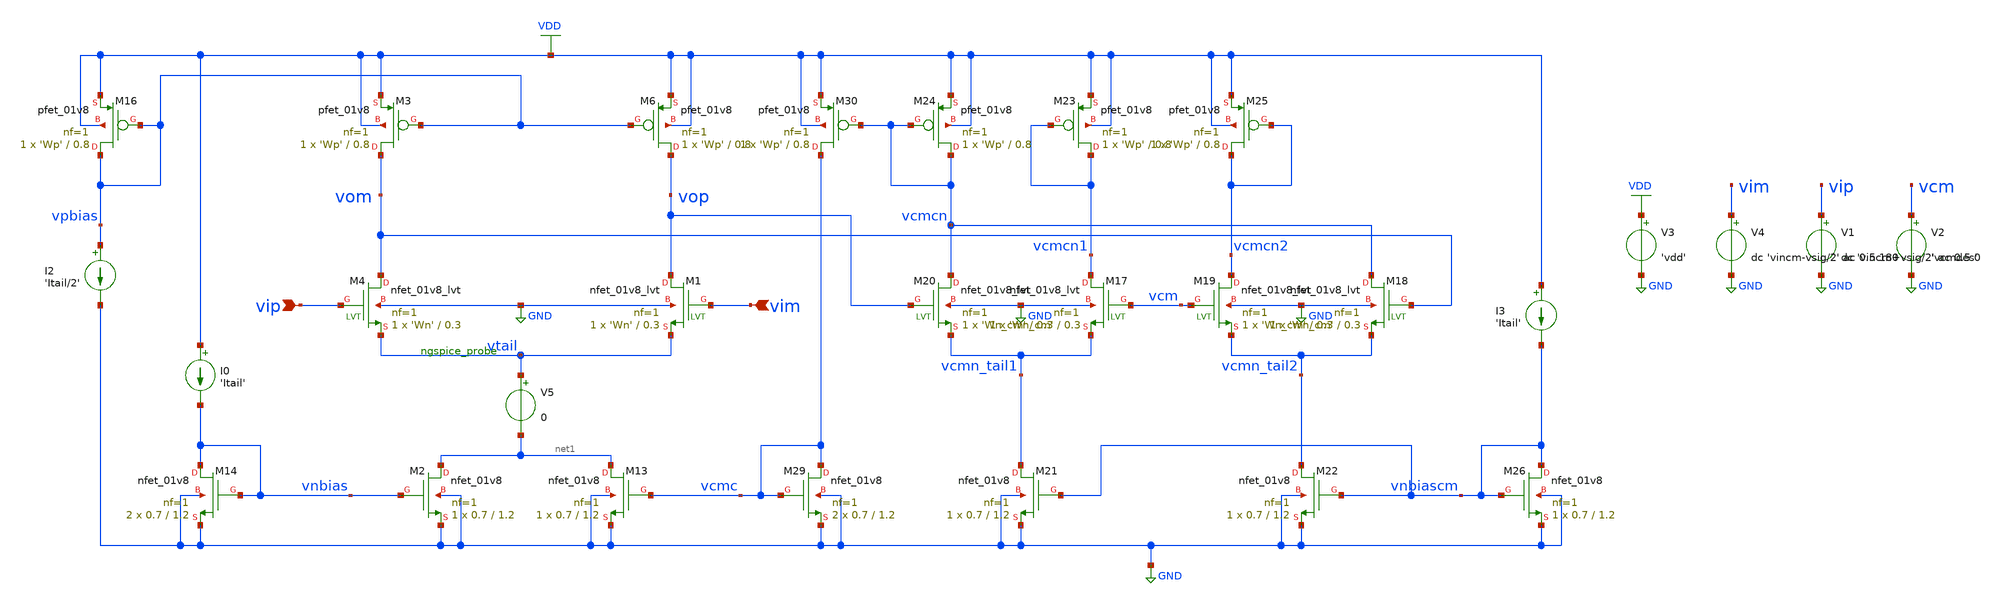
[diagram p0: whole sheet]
** sch_path: designs/diff_ota.sch
* Copyright 2020 Stefan Frederik Schippers
* Licensed under the Apache License, Version 2.0 (the "License");
* you may not use this file except in compliance with the License.
* You may obtain a copy of the License at
* https://www.apache.org/licenses/LICENSE-2.0
* Unless required by applicable law or agreed to in writing, software
* distributed under the License is distributed on an "AS IS" BASIS,
* WITHOUT WARRANTIES OR CONDITIONS OF ANY KIND, either express or implied.
* See the License for the specific language governing permissions and
* limitations under the License.
**.subckt diff_ota vip vim
*.ipin vip
*.ipin vim
V1 vip GND dc 'vincm+vsig/2' ac 0.5 0
V3 VDD GND 'vdd'
V4 vim GND dc 'vincm-vsig/2' ac 0.5 180
V5 vtail net1 0
XM6 vop vpbias VDD VDD sky130_fd_pr__pfet_01v8 L=0.8 W='Wp' nf=1 ad='int((nf+1)/2) * W/nf * 0.29' as='int((nf+2)/2) * W/nf * 0.29'
+ pd='2*int((nf+1)/2) * (W/nf + 0.29)' ps='2*int((nf+2)/2) * (W/nf + 0.29)' nrd='0.29 / W' nrs='0.29 / W'
+ sa=0 sb=0 sd=0 mult=1 m=1
XM3 vom vpbias VDD VDD sky130_fd_pr__pfet_01v8 L=0.8 W='Wp' nf=1 ad='int((nf+1)/2) * W/nf * 0.29' as='int((nf+2)/2) * W/nf * 0.29'
+ pd='2*int((nf+1)/2) * (W/nf + 0.29)' ps='2*int((nf+2)/2) * (W/nf + 0.29)' nrd='0.29 / W' nrs='0.29 / W'
+ sa=0 sb=0 sd=0 mult=1 m=1
XM2 net1 vnbias GND GND sky130_fd_pr__nfet_01v8 L=1.2 W=0.7 nf=1 ad='int((nf+1)/2) * W/nf * 0.29' as='int((nf+2)/2) * W/nf * 0.29'
+ pd='2*int((nf+1)/2) * (W/nf + 0.29)' ps='2*int((nf+2)/2) * (W/nf + 0.29)' nrd='0.29 / W' nrs='0.29 / W'
+ sa=0 sb=0 sd=0 mult=1 m=1
XM13 net1 vcmc GND GND sky130_fd_pr__nfet_01v8 L=1.2 W=0.7 nf=1 ad='int((nf+1)/2) * W/nf * 0.29' as='int((nf+2)/2) * W/nf * 0.29'
+ pd='2*int((nf+1)/2) * (W/nf + 0.29)' ps='2*int((nf+2)/2) * (W/nf + 0.29)' nrd='0.29 / W' nrs='0.29 / W'
+ sa=0 sb=0 sd=0 mult=1 m=1
I0 VDD vnbias 'Itail'
XM14 vnbias vnbias GND GND sky130_fd_pr__nfet_01v8 L=1.2 W=0.7 nf=1 ad='int((nf+1)/2) * W/nf * 0.29'
+ as='int((nf+2)/2) * W/nf * 0.29' pd='2*int((nf+1)/2) * (W/nf + 0.29)' ps='2*int((nf+2)/2) * (W/nf + 0.29)'
+ nrd='0.29 / W' nrs='0.29 / W' sa=0 sb=0 sd=0 mult=2 m=2
I2 vpbias GND 'Itail/2'
XM16 vpbias vpbias VDD VDD sky130_fd_pr__pfet_01v8 L=0.8 W='Wp' nf=1 ad='int((nf+1)/2) * W/nf * 0.29'
+ as='int((nf+2)/2) * W/nf * 0.29' pd='2*int((nf+1)/2) * (W/nf + 0.29)' ps='2*int((nf+2)/2) * (W/nf + 0.29)'
+ nrd='0.29 / W' nrs='0.29 / W' sa=0 sb=0 sd=0 mult=1 m=1
V2 vcm GND 'vcmdes'
XM21 vcmn_tail1 vnbiascm GND GND sky130_fd_pr__nfet_01v8 L=1.2 W=0.7 nf=1 ad='int((nf+1)/2) * W/nf * 0.29'
+ as='int((nf+2)/2) * W/nf * 0.29' pd='2*int((nf+1)/2) * (W/nf + 0.29)' ps='2*int((nf+2)/2) * (W/nf + 0.29)'
+ nrd='0.29 / W' nrs='0.29 / W' sa=0 sb=0 sd=0 mult=1 m=1
XM22 vcmn_tail2 vnbiascm GND GND sky130_fd_pr__nfet_01v8 L=1.2 W=0.7 nf=1 ad='int((nf+1)/2) * W/nf * 0.29'
+ as='int((nf+2)/2) * W/nf * 0.29' pd='2*int((nf+1)/2) * (W/nf + 0.29)' ps='2*int((nf+2)/2) * (W/nf + 0.29)'
+ nrd='0.29 / W' nrs='0.29 / W' sa=0 sb=0 sd=0 mult=1 m=1
XM23 vcmcn1 vcmcn1 VDD VDD sky130_fd_pr__pfet_01v8 L=0.8 W='Wp' nf=1 ad='int((nf+1)/2) * W/nf * 0.29'
+ as='int((nf+2)/2) * W/nf * 0.29' pd='2*int((nf+1)/2) * (W/nf + 0.29)' ps='2*int((nf+2)/2) * (W/nf + 0.29)'
+ nrd='0.29 / W' nrs='0.29 / W' sa=0 sb=0 sd=0 mult=1 m=1
XM24 vcmcn vcmcn VDD VDD sky130_fd_pr__pfet_01v8 L=0.8 W='Wp' nf=1 ad='int((nf+1)/2) * W/nf * 0.29' as='int((nf+2)/2) * W/nf * 0.29'
+ pd='2*int((nf+1)/2) * (W/nf + 0.29)' ps='2*int((nf+2)/2) * (W/nf + 0.29)' nrd='0.29 / W' nrs='0.29 / W'
+ sa=0 sb=0 sd=0 mult=1 m=1
I3 VDD vnbiascm 'Itail'
XM26 vnbiascm vnbiascm GND GND sky130_fd_pr__nfet_01v8 L=1.2 W=0.7 nf=1 ad='int((nf+1)/2) * W/nf * 0.29'
+ as='int((nf+2)/2) * W/nf * 0.29' pd='2*int((nf+1)/2) * (W/nf + 0.29)' ps='2*int((nf+2)/2) * (W/nf + 0.29)'
+ nrd='0.29 / W' nrs='0.29 / W' sa=0 sb=0 sd=0 mult=1 m=1
XM20 vcmcn vop vcmn_tail1 GND sky130_fd_pr__nfet_01v8_lvt L=0.3 W='Wn_cm' nf=1 ad='int((nf+1)/2) * W/nf * 0.29'
+ as='int((nf+2)/2) * W/nf * 0.29' pd='2*int((nf+1)/2) * (W/nf + 0.29)' ps='2*int((nf+2)/2) * (W/nf + 0.29)'
+ nrd='0.29 / W' nrs='0.29 / W' sa=0 sb=0 sd=0 mult=1 m=1
XM17 vcmcn1 vcm vcmn_tail1 GND sky130_fd_pr__nfet_01v8_lvt L=0.3 W='Wn_cm' nf=1 ad='int((nf+1)/2) * W/nf * 0.29'
+ as='int((nf+2)/2) * W/nf * 0.29' pd='2*int((nf+1)/2) * (W/nf + 0.29)' ps='2*int((nf+2)/2) * (W/nf + 0.29)'
+ nrd='0.29 / W' nrs='0.29 / W' sa=0 sb=0 sd=0 mult=1 m=1
XM18 vcmcn vom vcmn_tail2 GND sky130_fd_pr__nfet_01v8_lvt L=0.3 W='Wn_cm' nf=1 ad='int((nf+1)/2) * W/nf * 0.29'
+ as='int((nf+2)/2) * W/nf * 0.29' pd='2*int((nf+1)/2) * (W/nf + 0.29)' ps='2*int((nf+2)/2) * (W/nf + 0.29)'
+ nrd='0.29 / W' nrs='0.29 / W' sa=0 sb=0 sd=0 mult=1 m=1
XM19 vcmcn2 vcm vcmn_tail2 GND sky130_fd_pr__nfet_01v8_lvt L=0.3 W='Wn_cm' nf=1 ad='int((nf+1)/2) * W/nf * 0.29'
+ as='int((nf+2)/2) * W/nf * 0.29' pd='2*int((nf+1)/2) * (W/nf + 0.29)' ps='2*int((nf+2)/2) * (W/nf + 0.29)'
+ nrd='0.29 / W' nrs='0.29 / W' sa=0 sb=0 sd=0 mult=1 m=1
XM4 vom vip vtail GND sky130_fd_pr__nfet_01v8_lvt L=0.3 W='Wn' nf=1 ad='int((nf+1)/2) * W/nf * 0.29'
+ as='int((nf+2)/2) * W/nf * 0.29' pd='2*int((nf+1)/2) * (W/nf + 0.29)' ps='2*int((nf+2)/2) * (W/nf + 0.29)'
+ nrd='0.29 / W' nrs='0.29 / W' sa=0 sb=0 sd=0 mult=1 m=1
XM1 vop vim vtail GND sky130_fd_pr__nfet_01v8_lvt L=0.3 W='Wn' nf=1 ad='int((nf+1)/2) * W/nf * 0.29'
+ as='int((nf+2)/2) * W/nf * 0.29' pd='2*int((nf+1)/2) * (W/nf + 0.29)' ps='2*int((nf+2)/2) * (W/nf + 0.29)'
+ nrd='0.29 / W' nrs='0.29 / W' sa=0 sb=0 sd=0 mult=1 m=1
XM29 vcmc vcmc GND GND sky130_fd_pr__nfet_01v8 L=1.2 W=0.7 nf=1 ad='int((nf+1)/2) * W/nf * 0.29' as='int((nf+2)/2) * W/nf * 0.29'
+ pd='2*int((nf+1)/2) * (W/nf + 0.29)' ps='2*int((nf+2)/2) * (W/nf + 0.29)' nrd='0.29 / W' nrs='0.29 / W'
+ sa=0 sb=0 sd=0 mult=2 m=2
XM30 vcmc vcmcn VDD VDD sky130_fd_pr__pfet_01v8 L=0.8 W='Wp' nf=1 ad='int((nf+1)/2) * W/nf * 0.29' as='int((nf+2)/2) * W/nf * 0.29'
+ pd='2*int((nf+1)/2) * (W/nf + 0.29)' ps='2*int((nf+2)/2) * (W/nf + 0.29)' nrd='0.29 / W' nrs='0.29 / W'
+ sa=0 sb=0 sd=0 mult=1 m=1
XM25 vcmcn2 vcmcn2 VDD VDD sky130_fd_pr__pfet_01v8 L=0.8 W='Wp' nf=1 ad='int((nf+1)/2) * W/nf * 0.29'
+ as='int((nf+2)/2) * W/nf * 0.29' pd='2*int((nf+1)/2) * (W/nf + 0.29)' ps='2*int((nf+2)/2) * (W/nf + 0.29)'
+ nrd='0.29 / W' nrs='0.29 / W' sa=0 sb=0 sd=0 mult=1 m=1
**** begin user architecture code

.include $::SKYWATER_MODELS/cells/nfet_01v8/sky130_fd_pr__nfet_01v8__tt.corner.spice
.include $::SKYWATER_MODELS/cells/nfet_01v8_lvt/sky130_fd_pr__nfet_01v8_lvt__tt.corner.spice
.include $::SKYWATER_MODELS/cells/pfet_01v8/sky130_fd_pr__pfet_01v8__tt.corner.spice
.include $::SKYWATER_MODELS/cells/nfet_03v3_nvt/sky130_fd_pr__nfet_03v3_nvt__tt.corner.spice
.include $::SKYWATER_MODELS/cells/nfet_05v0_nvt/sky130_fd_pr__nfet_05v0_nvt__tt.corner.spice
.include $::SKYWATER_MODELS/cells/esd_nfet_01v8/sky130_fd_pr__esd_nfet_01v8__tt.corner.spice
.include $::SKYWATER_MODELS/cells/pfet_01v8_lvt/sky130_fd_pr__pfet_01v8_lvt__tt.corner.spice
.include $::SKYWATER_MODELS/cells/pfet_01v8_hvt/sky130_fd_pr__pfet_01v8_hvt__tt.corner.spice
.include $::SKYWATER_MODELS/cells/esd_pfet_g5v0d10v5/sky130_fd_pr__esd_pfet_g5v0d10v5__tt.corner.spice
.include $::SKYWATER_MODELS/cells/pfet_g5v0d10v5/sky130_fd_pr__pfet_g5v0d10v5__tt.corner.spice
.include $::SKYWATER_MODELS/cells/pfet_g5v0d16v0/sky130_fd_pr__pfet_g5v0d16v0__tt.corner.spice
.include $::SKYWATER_MODELS/cells/nfet_g5v0d10v5/sky130_fd_pr__nfet_g5v0d10v5__tt.corner.spice
.include $::SKYWATER_MODELS/cells/nfet_g5v0d16v0/sky130_fd_pr__nfet_g5v0d16v0__tt_discrete.corner.spice
.include $::SKYWATER_MODELS/cells/esd_nfet_g5v0d10v5/sky130_fd_pr__esd_nfet_g5v0d10v5__tt.corner.spice
.include $::SKYWATER_MODELS/models/corners/tt/nonfet.spice
* Mismatch parameters
.include $::SKYWATER_MODELS/cells/nfet_01v8/sky130_fd_pr__nfet_01v8__mismatch.corner.spice
.include $::SKYWATER_MODELS/cells/pfet_01v8/sky130_fd_pr__pfet_01v8__mismatch.corner.spice
.include $::SKYWATER_MODELS/cells/nfet_01v8_lvt/sky130_fd_pr__nfet_01v8_lvt__mismatch.corner.spice
.include $::SKYWATER_MODELS/cells/pfet_01v8_lvt/sky130_fd_pr__pfet_01v8_lvt__mismatch.corner.spice
.include $::SKYWATER_MODELS/cells/pfet_01v8_hvt/sky130_fd_pr__pfet_01v8_hvt__mismatch.corner.spice
.include $::SKYWATER_MODELS/cells/nfet_g5v0d10v5/sky130_fd_pr__nfet_g5v0d10v5__mismatch.corner.spice
.include $::SKYWATER_MODELS/cells/pfet_g5v0d10v5/sky130_fd_pr__pfet_g5v0d10v5__mismatch.corner.spice
.include $::SKYWATER_MODELS/cells/nfet_05v0_nvt/sky130_fd_pr__nfet_05v0_nvt__mismatch.corner.spice
.include $::SKYWATER_MODELS/cells/nfet_03v3_nvt/sky130_fd_pr__nfet_03v3_nvt__mismatch.corner.spice
* Resistor$::SKYWATER_MODELS/Capacitor
.include $::SKYWATER_MODELS/models/r+c/res_typical__cap_typical.spice
.include $::SKYWATER_MODELS/models/r+c/res_typical__cap_typical__lin.spice
* Special cells
.include $::SKYWATER_MODELS/models/corners/tt/specialized_cells.spice
* All models
.include $::SKYWATER_MODELS/models/all.spice
* Corner
.include $::SKYWATER_MODELS/models/corners/tt/rf.spice

**** end user architecture code
**.ends
.GLOBAL VDD
.GLOBAL GND
**** begin user architecture code

.include diff_ota_commands.spice

**** end user architecture code
.end
